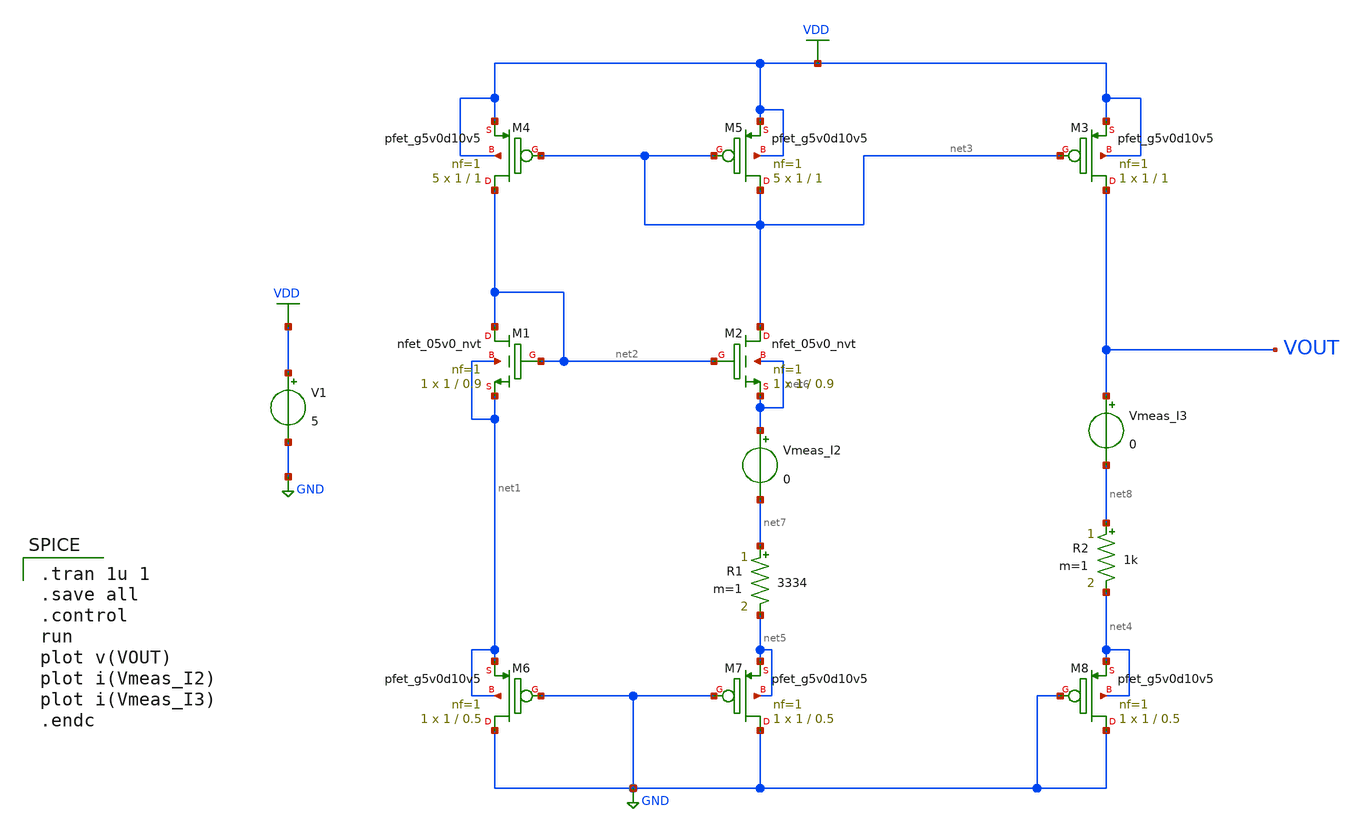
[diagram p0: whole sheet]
** sch_path: Circuits/Examples/Analog/BGR/BGR_1.2v.sch
**.subckt BGR_1.2v
XM1 net2 net2 net1 net1 sky130_fd_pr__nfet_05v0_nvt L=0.9 W=1 nf=1 ad='int((nf+1)/2) * W/nf * 0.29' as='int((nf+2)/2) * W/nf * 0.29'
+ pd='2*int((nf+1)/2) * (W/nf + 0.29)' ps='2*int((nf+2)/2) * (W/nf + 0.29)' nrd='0.29 / W' nrs='0.29 / W'
+ sa=0 sb=0 sd=0 mult=1 m=1
XM2 net3 net2 net6 net6 sky130_fd_pr__nfet_05v0_nvt L=0.9 W=1 nf=1 ad='int((nf+1)/2) * W/nf * 0.29' as='int((nf+2)/2) * W/nf * 0.29'
+ pd='2*int((nf+1)/2) * (W/nf + 0.29)' ps='2*int((nf+2)/2) * (W/nf + 0.29)' nrd='0.29 / W' nrs='0.29 / W'
+ sa=0 sb=0 sd=0 mult=1 m=1
XM4 net2 net3 VDD VDD sky130_fd_pr__pfet_g5v0d10v5 L=1 W=1 nf=1 ad='int((nf+1)/2) * W/nf * 0.29' as='int((nf+2)/2) * W/nf * 0.29'
+ pd='2*int((nf+1)/2) * (W/nf + 0.29)' ps='2*int((nf+2)/2) * (W/nf + 0.29)' nrd='0.29 / W' nrs='0.29 / W'
+ sa=0 sb=0 sd=0 mult=5 m=5
XM5 net3 net3 VDD VDD sky130_fd_pr__pfet_g5v0d10v5 L=1 W=1 nf=1 ad='int((nf+1)/2) * W/nf * 0.29' as='int((nf+2)/2) * W/nf * 0.29'
+ pd='2*int((nf+1)/2) * (W/nf + 0.29)' ps='2*int((nf+2)/2) * (W/nf + 0.29)' nrd='0.29 / W' nrs='0.29 / W'
+ sa=0 sb=0 sd=0 mult=5 m=5
R1 net7 net5 3334 m=1
XM3 VOUT net3 VDD VDD sky130_fd_pr__pfet_g5v0d10v5 L=1 W=1 nf=1 ad='int((nf+1)/2) * W/nf * 0.29' as='int((nf+2)/2) * W/nf * 0.29'
+ pd='2*int((nf+1)/2) * (W/nf + 0.29)' ps='2*int((nf+2)/2) * (W/nf + 0.29)' nrd='0.29 / W' nrs='0.29 / W'
+ sa=0 sb=0 sd=0 mult=1 m=1
R2 net8 net4 1k m=1
V1 VDD GND 5
Vmeas_I2 net6 net7 0
Vmeas_I3 VOUT net8 0
XM6 GND GND net1 net1 sky130_fd_pr__pfet_g5v0d10v5 L=0.5 W=1 nf=1 ad='int((nf+1)/2) * W/nf * 0.29' as='int((nf+2)/2) * W/nf * 0.29'
+ pd='2*int((nf+1)/2) * (W/nf + 0.29)' ps='2*int((nf+2)/2) * (W/nf + 0.29)' nrd='0.29 / W' nrs='0.29 / W'
+ sa=0 sb=0 sd=0 mult=1 m=1
XM7 GND GND net5 net5 sky130_fd_pr__pfet_g5v0d10v5 L=0.5 W=1 nf=1 ad='int((nf+1)/2) * W/nf * 0.29' as='int((nf+2)/2) * W/nf * 0.29'
+ pd='2*int((nf+1)/2) * (W/nf + 0.29)' ps='2*int((nf+2)/2) * (W/nf + 0.29)' nrd='0.29 / W' nrs='0.29 / W'
+ sa=0 sb=0 sd=0 mult=1 m=1
XM8 GND GND net4 net4 sky130_fd_pr__pfet_g5v0d10v5 L=0.5 W=1 nf=1 ad='int((nf+1)/2) * W/nf * 0.29' as='int((nf+2)/2) * W/nf * 0.29'
+ pd='2*int((nf+1)/2) * (W/nf + 0.29)' ps='2*int((nf+2)/2) * (W/nf + 0.29)' nrd='0.29 / W' nrs='0.29 / W'
+ sa=0 sb=0 sd=0 mult=1 m=1
**** begin user architecture code
 ** manual skywater pdks install (with patches applied)
* .lib $::SKYWATER_MODELS/models/sky130.lib.spice tt

** opencircuitdesign pdks install
.lib $::SKYWATER_MODELS/sky130.lib.spice tt

.param mc_mm_switch=0
.param mc_pr_switch=0


.tran 1u 1
.save all
.control
run
plot v(VOUT)
plot i(Vmeas_I2)
plot i(Vmeas_I3)
.endc


**** end user architecture code
**.ends
.GLOBAL GND
.GLOBAL VDD
.end
